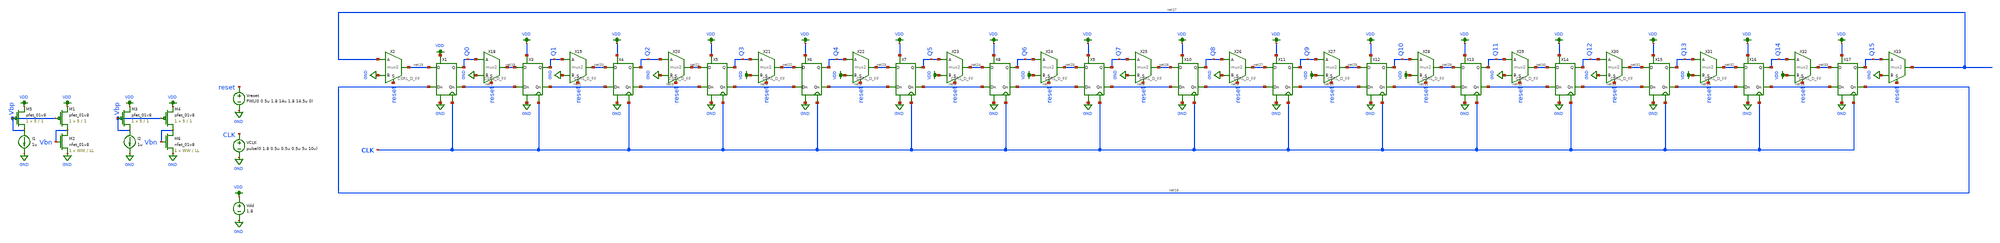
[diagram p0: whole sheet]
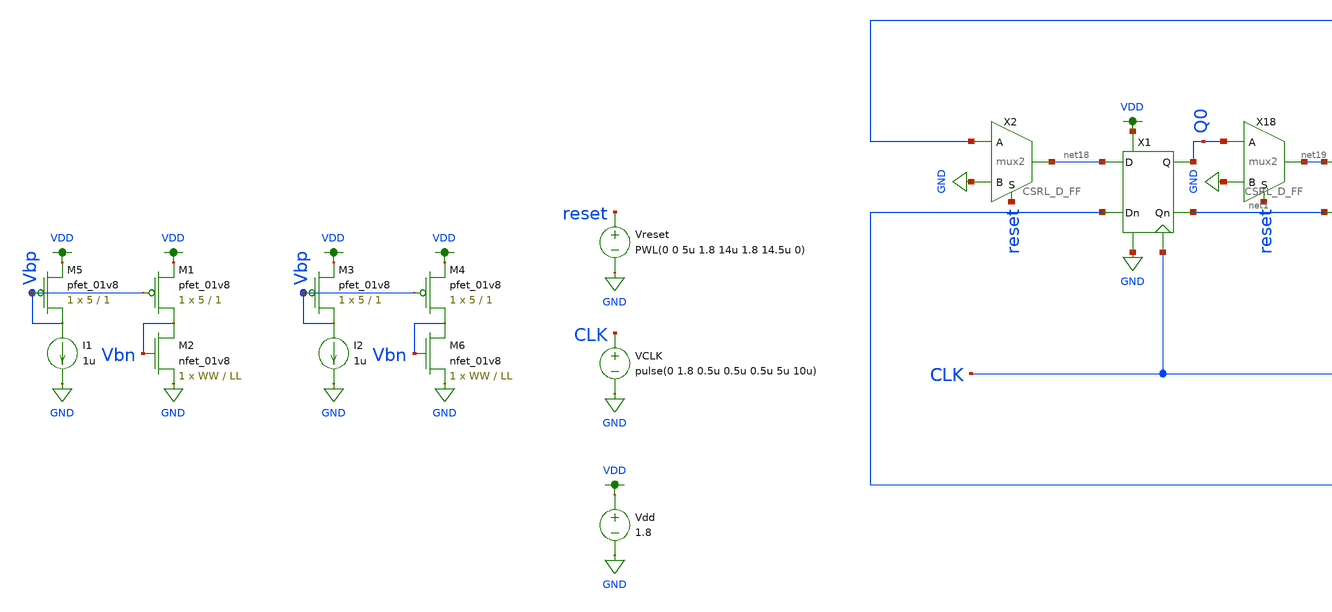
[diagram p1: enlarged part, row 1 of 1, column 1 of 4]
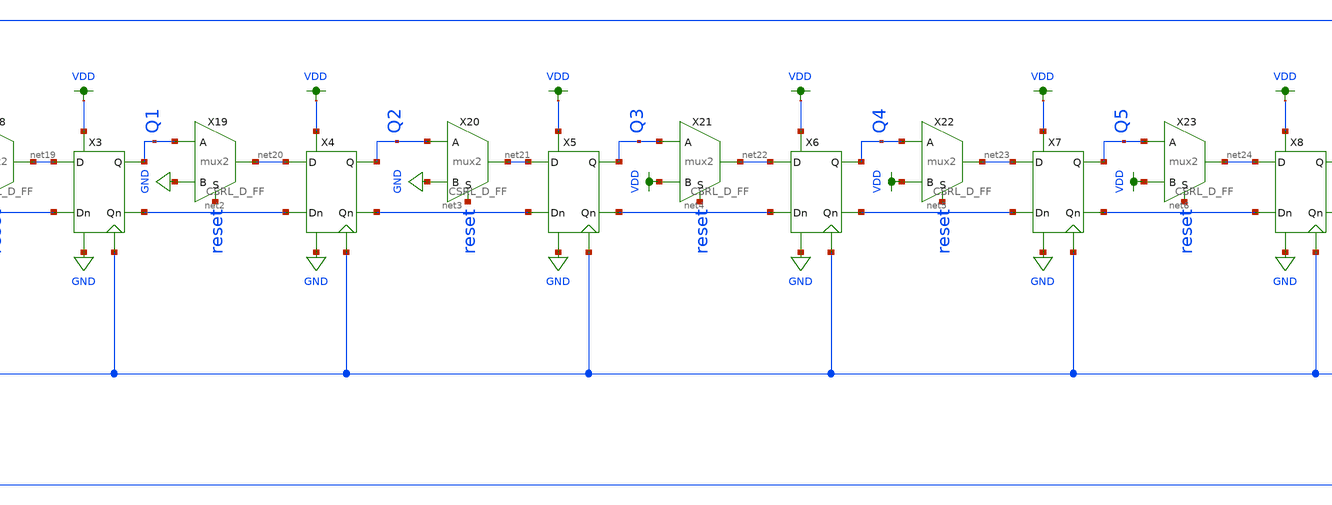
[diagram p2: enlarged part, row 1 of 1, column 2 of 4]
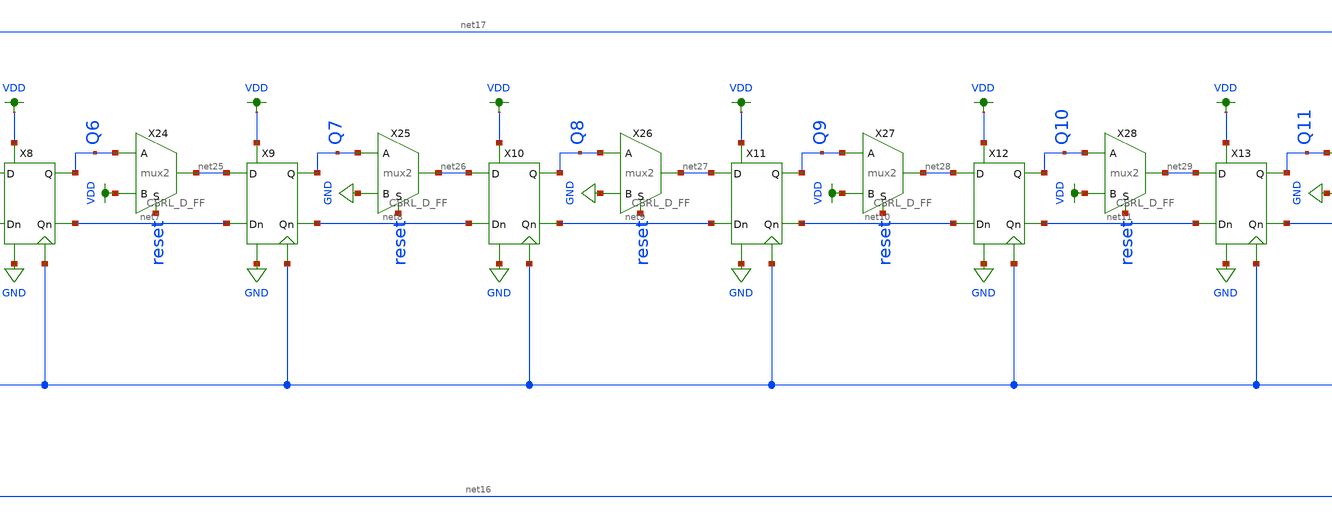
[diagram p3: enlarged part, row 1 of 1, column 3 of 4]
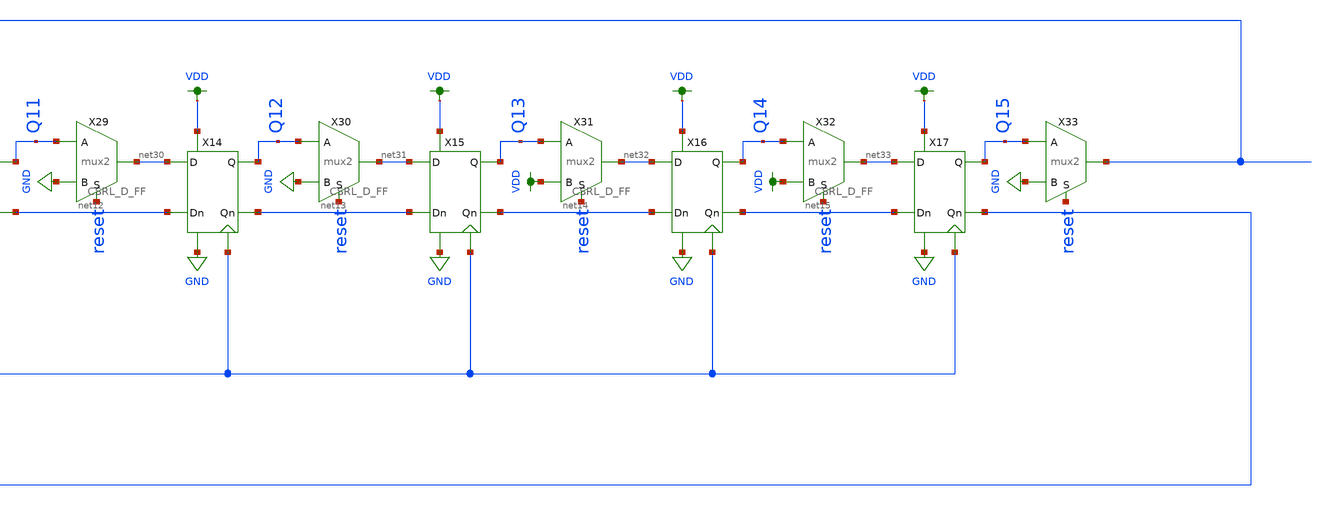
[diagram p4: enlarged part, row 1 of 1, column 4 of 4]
** sch_path: schematic/archive/phi1-new-circular-new.sch
**.subckt phi1-new-circular-new
VCLK CLK GND pulse(0 1.8 0.5u 0.5u 0.5u 5u 10u)
Vdd VDD GND 1.8
X3 net1 net19 net2 Q1 GND VDD CLK CSRL_D_FF
X4 net2 net20 net3 Q2 GND VDD CLK CSRL_D_FF
X5 net3 net21 net4 Q3 GND VDD CLK CSRL_D_FF
X6 net4 net22 net5 Q4 GND VDD CLK CSRL_D_FF
X7 net5 net23 net6 Q5 GND VDD CLK CSRL_D_FF
X8 net6 net24 net7 Q6 GND VDD CLK CSRL_D_FF
X9 net7 net25 net8 Q7 GND VDD CLK CSRL_D_FF
X10 net8 net26 net9 Q8 GND VDD CLK CSRL_D_FF
X11 net9 net27 net10 Q9 GND VDD CLK CSRL_D_FF
X12 net10 net28 net11 Q10 GND VDD CLK CSRL_D_FF
X13 net11 net29 net12 Q11 GND VDD CLK CSRL_D_FF
X14 net12 net30 net13 Q12 GND VDD CLK CSRL_D_FF
X15 net13 net31 net14 Q13 GND VDD CLK CSRL_D_FF
X16 net14 net32 net15 Q14 GND VDD CLK CSRL_D_FF
X17 net15 net33 net16 Q15 GND VDD CLK CSRL_D_FF
X1 net16 net18 net1 Q0 GND VDD CLK CSRL_D_FF
X2 net18 net17 GND reset mux2
X18 net19 Q0 GND reset mux2
X19 net20 Q1 GND reset mux2
X20 net21 Q2 GND reset mux2
X21 net22 Q3 VDD reset mux2
X22 net23 Q4 VDD reset mux2
X23 net24 Q5 VDD reset mux2
X24 net25 Q6 VDD reset mux2
X25 net26 Q7 GND reset mux2
X26 net27 Q8 GND reset mux2
X27 net28 Q9 VDD reset mux2
X28 net29 Q10 VDD reset mux2
X29 net30 Q11 GND reset mux2
X30 net31 Q12 GND reset mux2
X31 net32 Q13 VDD reset mux2
X32 net33 Q14 VDD reset mux2
X33 net17 Q15 GND reset mux2
XM5 Vbp Vbp VDD VDD sky130_fd_pr__pfet_01v8 L=1 W=5 nf=1 ad='int((nf+1)/2) * W/nf * 0.29' as='int((nf+2)/2) * W/nf * 0.29'
+ pd='2*int((nf+1)/2) * (W/nf + 0.29)' ps='2*int((nf+2)/2) * (W/nf + 0.29)' nrd='0.29 / W' nrs='0.29 / W'
+ sa=0 sb=0 sd=0 mult=1 m=1
I1 Vbp GND 1u
XM1 Vbn Vbp VDD VDD sky130_fd_pr__pfet_01v8 L=1 W=5 nf=1 ad='int((nf+1)/2) * W/nf * 0.29' as='int((nf+2)/2) * W/nf * 0.29'
+ pd='2*int((nf+1)/2) * (W/nf + 0.29)' ps='2*int((nf+2)/2) * (W/nf + 0.29)' nrd='0.29 / W' nrs='0.29 / W'
+ sa=0 sb=0 sd=0 mult=1 m=1
XM2 Vbn Vbn GND GND sky130_fd_pr__nfet_01v8 L=LL W=WW nf=1 ad='int((nf+1)/2) * W/nf * 0.29' as='int((nf+2)/2) * W/nf * 0.29'
+ pd='2*int((nf+1)/2) * (W/nf + 0.29)' ps='2*int((nf+2)/2) * (W/nf + 0.29)' nrd='0.29 / W' nrs='0.29 / W'
+ sa=0 sb=0 sd=0 mult=1 m=1
XM3 Vbp Vbp VDD VDD sky130_fd_pr__pfet_01v8 L=1 W=5 nf=1 ad='int((nf+1)/2) * W/nf * 0.29' as='int((nf+2)/2) * W/nf * 0.29'
+ pd='2*int((nf+1)/2) * (W/nf + 0.29)' ps='2*int((nf+2)/2) * (W/nf + 0.29)' nrd='0.29 / W' nrs='0.29 / W'
+ sa=0 sb=0 sd=0 mult=1 m=1
I2 Vbp GND 1u
XM4 Vbn Vbp VDD VDD sky130_fd_pr__pfet_01v8 L=1 W=5 nf=1 ad='int((nf+1)/2) * W/nf * 0.29' as='int((nf+2)/2) * W/nf * 0.29'
+ pd='2*int((nf+1)/2) * (W/nf + 0.29)' ps='2*int((nf+2)/2) * (W/nf + 0.29)' nrd='0.29 / W' nrs='0.29 / W'
+ sa=0 sb=0 sd=0 mult=1 m=1
XM6 Vbn Vbn GND GND sky130_fd_pr__nfet_01v8 L=LL W=WW nf=1 ad='int((nf+1)/2) * W/nf * 0.29' as='int((nf+2)/2) * W/nf * 0.29'
+ pd='2*int((nf+1)/2) * (W/nf + 0.29)' ps='2*int((nf+2)/2) * (W/nf + 0.29)' nrd='0.29 / W' nrs='0.29 / W'
+ sa=0 sb=0 sd=0 mult=1 m=1
Vreset reset GND PWL(0 0 5u 1.8 14u 1.8 14.5u 0)
**** begin user architecture code

.ic v(Q0)=0 v(Q1)=0 v(Q2)=0 v(Q3)=0 v(Q4)=1 v(Q5)=1 v(Q6)=1 v(Q7)=1 v(Q8)=0 v(Q9)=0 v(Q10)=1
+ v(Q11)=1 v(Q12)=0 v(Q13)=0 v(Q14)=1 v(Q15)=1
.tran 0.5u 50u
.save all


.option wnflag=1
.param MC_SWITCH=0.0
.lib ~/skywater/skywater-pdk/libraries/sky130_fd_pr_ngspice/latest/models/sky130.lib.spice tt

**** end user architecture code
**.ends

* expanding   symbol:  /home/madvlsi/Documents/MADVLSI-Final_Project/schematic/CSRL_D_FF.sym # of
*+ pins=7
** sym_path: schematic/CSRL_D_FF.sym
** sch_path: schematic/CSRL_D_FF.sch
.subckt CSRL_D_FF Dn D Qn Q VN VP CLK
*.ipin Dn
*.ipin D
*.iopin VP
*.iopin VN
*.iopin CLK
*.opin Qn
*.opin Q
XM1 net5 CLK VP VDD sky130_fd_pr__pfet_01v8 L=0.15 W=1 nf=1 ad='int((nf+1)/2) * W/nf * 0.29' as='int((nf+2)/2) * W/nf * 0.29'
+ pd='2*int((nf+1)/2) * (W/nf + 0.29)' ps='2*int((nf+2)/2) * (W/nf + 0.29)' nrd='0.29 / W' nrs='0.29 / W'
+ sa=0 sb=0 sd=0 mult=1 m=1
XM2 net6 CLK VP VDD sky130_fd_pr__pfet_01v8 L=0.15 W=1 nf=1 ad='int((nf+1)/2) * W/nf * 0.29' as='int((nf+2)/2) * W/nf * 0.29'
+ pd='2*int((nf+1)/2) * (W/nf + 0.29)' ps='2*int((nf+2)/2) * (W/nf + 0.29)' nrd='0.29 / W' nrs='0.29 / W'
+ sa=0 sb=0 sd=0 mult=1 m=1
XM3 net3 CLK Q GND sky130_fd_pr__nfet_01v8 L=0.15 W=1 nf=1 ad='int((nf+1)/2) * W/nf * 0.29' as='int((nf+2)/2) * W/nf * 0.29'
+ pd='2*int((nf+1)/2) * (W/nf + 0.29)' ps='2*int((nf+2)/2) * (W/nf + 0.29)' nrd='0.29 / W' nrs='0.29 / W'
+ sa=0 sb=0 sd=0 mult=1 m=1
XM4 net4 CLK Qn GND sky130_fd_pr__nfet_01v8 L=0.15 W=1 nf=1 ad='int((nf+1)/2) * W/nf * 0.29' as='int((nf+2)/2) * W/nf * 0.29'
+ pd='2*int((nf+1)/2) * (W/nf + 0.29)' ps='2*int((nf+2)/2) * (W/nf + 0.29)' nrd='0.29 / W' nrs='0.29 / W'
+ sa=0 sb=0 sd=0 mult=1 m=1
XM5 Q Qn net6 VDD sky130_fd_pr__pfet_01v8 L=0.15 W=1 nf=1 ad='int((nf+1)/2) * W/nf * 0.29' as='int((nf+2)/2) * W/nf * 0.29'
+ pd='2*int((nf+1)/2) * (W/nf + 0.29)' ps='2*int((nf+2)/2) * (W/nf + 0.29)' nrd='0.29 / W' nrs='0.29 / W'
+ sa=0 sb=0 sd=0 mult=1 m=1
XM6 VN Qn Q GND sky130_fd_pr__nfet_01v8 L=0.15 W=1 nf=1 ad='int((nf+1)/2) * W/nf * 0.29' as='int((nf+2)/2) * W/nf * 0.29'
+ pd='2*int((nf+1)/2) * (W/nf + 0.29)' ps='2*int((nf+2)/2) * (W/nf + 0.29)' nrd='0.29 / W' nrs='0.29 / W'
+ sa=0 sb=0 sd=0 mult=1 m=1
XM7 Qn Q net5 VDD sky130_fd_pr__pfet_01v8 L=0.15 W=1 nf=1 ad='int((nf+1)/2) * W/nf * 0.29' as='int((nf+2)/2) * W/nf * 0.29'
+ pd='2*int((nf+1)/2) * (W/nf + 0.29)' ps='2*int((nf+2)/2) * (W/nf + 0.29)' nrd='0.29 / W' nrs='0.29 / W'
+ sa=0 sb=0 sd=0 mult=1 m=1
XM8 VN Q Qn GND sky130_fd_pr__nfet_01v8 L=0.15 W=1 nf=1 ad='int((nf+1)/2) * W/nf * 0.29' as='int((nf+2)/2) * W/nf * 0.29'
+ pd='2*int((nf+1)/2) * (W/nf + 0.29)' ps='2*int((nf+2)/2) * (W/nf + 0.29)' nrd='0.29 / W' nrs='0.29 / W'
+ sa=0 sb=0 sd=0 mult=1 m=1
XM9 net4 CLK Dn VDD sky130_fd_pr__pfet_01v8 L=0.15 W=1 nf=1 ad='int((nf+1)/2) * W/nf * 0.29' as='int((nf+2)/2) * W/nf * 0.29'
+ pd='2*int((nf+1)/2) * (W/nf + 0.29)' ps='2*int((nf+2)/2) * (W/nf + 0.29)' nrd='0.29 / W' nrs='0.29 / W'
+ sa=0 sb=0 sd=0 mult=1 m=1
XM10 net3 CLK D VDD sky130_fd_pr__pfet_01v8 L=0.15 W=1 nf=1 ad='int((nf+1)/2) * W/nf * 0.29' as='int((nf+2)/2) * W/nf * 0.29'
+ pd='2*int((nf+1)/2) * (W/nf + 0.29)' ps='2*int((nf+2)/2) * (W/nf + 0.29)' nrd='0.29 / W' nrs='0.29 / W'
+ sa=0 sb=0 sd=0 mult=1 m=1
XM11 VN CLK net1 GND sky130_fd_pr__nfet_01v8 L=0.15 W=1 nf=1 ad='int((nf+1)/2) * W/nf * 0.29' as='int((nf+2)/2) * W/nf * 0.29'
+ pd='2*int((nf+1)/2) * (W/nf + 0.29)' ps='2*int((nf+2)/2) * (W/nf + 0.29)' nrd='0.29 / W' nrs='0.29 / W'
+ sa=0 sb=0 sd=0 mult=1 m=1
XM12 VN CLK net2 GND sky130_fd_pr__nfet_01v8 L=0.15 W=1 nf=1 ad='int((nf+1)/2) * W/nf * 0.29' as='int((nf+2)/2) * W/nf * 0.29'
+ pd='2*int((nf+1)/2) * (W/nf + 0.29)' ps='2*int((nf+2)/2) * (W/nf + 0.29)' nrd='0.29 / W' nrs='0.29 / W'
+ sa=0 sb=0 sd=0 mult=1 m=1
XM13 VP net3 net4 VDD sky130_fd_pr__pfet_01v8 L=0.15 W=1 nf=1 ad='int((nf+1)/2) * W/nf * 0.29' as='int((nf+2)/2) * W/nf * 0.29'
+ pd='2*int((nf+1)/2) * (W/nf + 0.29)' ps='2*int((nf+2)/2) * (W/nf + 0.29)' nrd='0.29 / W' nrs='0.29 / W'
+ sa=0 sb=0 sd=0 mult=1 m=1
XM14 VP net4 net3 VDD sky130_fd_pr__pfet_01v8 L=0.15 W=1 nf=1 ad='int((nf+1)/2) * W/nf * 0.29' as='int((nf+2)/2) * W/nf * 0.29'
+ pd='2*int((nf+1)/2) * (W/nf + 0.29)' ps='2*int((nf+2)/2) * (W/nf + 0.29)' nrd='0.29 / W' nrs='0.29 / W'
+ sa=0 sb=0 sd=0 mult=1 m=1
XM15 net3 net4 net1 GND sky130_fd_pr__nfet_01v8 L=0.15 W=1 nf=1 ad='int((nf+1)/2) * W/nf * 0.29' as='int((nf+2)/2) * W/nf * 0.29'
+ pd='2*int((nf+1)/2) * (W/nf + 0.29)' ps='2*int((nf+2)/2) * (W/nf + 0.29)' nrd='0.29 / W' nrs='0.29 / W'
+ sa=0 sb=0 sd=0 mult=1 m=1
XM16 net4 net3 net2 GND sky130_fd_pr__nfet_01v8 L=0.15 W=1 nf=1 ad='int((nf+1)/2) * W/nf * 0.29' as='int((nf+2)/2) * W/nf * 0.29'
+ pd='2*int((nf+1)/2) * (W/nf + 0.29)' ps='2*int((nf+2)/2) * (W/nf + 0.29)' nrd='0.29 / W' nrs='0.29 / W'
+ sa=0 sb=0 sd=0 mult=1 m=1
XM17 VN CLK net2 GND sky130_fd_pr__nfet_01v8 L=0.15 W=1 nf=1 ad='int((nf+1)/2) * W/nf * 0.29' as='int((nf+2)/2) * W/nf * 0.29'
+ pd='2*int((nf+1)/2) * (W/nf + 0.29)' ps='2*int((nf+2)/2) * (W/nf + 0.29)' nrd='0.29 / W' nrs='0.29 / W'
+ sa=0 sb=0 sd=0 mult=1 m=1
XM18 VN CLK net1 GND sky130_fd_pr__nfet_01v8 L=0.15 W=1 nf=1 ad='int((nf+1)/2) * W/nf * 0.29' as='int((nf+2)/2) * W/nf * 0.29'
+ pd='2*int((nf+1)/2) * (W/nf + 0.29)' ps='2*int((nf+2)/2) * (W/nf + 0.29)' nrd='0.29 / W' nrs='0.29 / W'
+ sa=0 sb=0 sd=0 mult=1 m=1
.ends


* expanding   symbol:  /home/madvlsi/Documents/MADVLSI-Final_Project/schematic/mux2.sym # of pins=4
** sym_path: /home/madvlsi/Documents/MADVLSI-Final_Project/schematic/mux2.sym
** sch_path: /home/madvlsi/Documents/MADVLSI-Final_Project/schematic/mux2.sch
.subckt mux2 Y A B S
*.opin Y
*.ipin B
*.ipin A
*.ipin S
XM1 Y net1 A VDD sky130_fd_pr__pfet_01v8 L=0.15 W=1 nf=1 ad='int((nf+1)/2) * W/nf * 0.29' as='int((nf+2)/2) * W/nf * 0.29'
+ pd='2*int((nf+1)/2) * (W/nf + 0.29)' ps='2*int((nf+2)/2) * (W/nf + 0.29)' nrd='0.29 / W' nrs='0.29 / W'
+ sa=0 sb=0 sd=0 mult=1 m=1
XM2 Y S B VDD sky130_fd_pr__pfet_01v8 L=0.15 W=1 nf=1 ad='int((nf+1)/2) * W/nf * 0.29' as='int((nf+2)/2) * W/nf * 0.29'
+ pd='2*int((nf+1)/2) * (W/nf + 0.29)' ps='2*int((nf+2)/2) * (W/nf + 0.29)' nrd='0.29 / W' nrs='0.29 / W'
+ sa=0 sb=0 sd=0 mult=1 m=1
XM3 Y net1 B GND sky130_fd_pr__nfet_01v8 L=0.15 W=1 nf=1 ad='int((nf+1)/2) * W/nf * 0.29' as='int((nf+2)/2) * W/nf * 0.29'
+ pd='2*int((nf+1)/2) * (W/nf + 0.29)' ps='2*int((nf+2)/2) * (W/nf + 0.29)' nrd='0.29 / W' nrs='0.29 / W'
+ sa=0 sb=0 sd=0 mult=1 m=1
XM4 Y S A GND sky130_fd_pr__nfet_01v8 L=0.15 W=1 nf=1 ad='int((nf+1)/2) * W/nf * 0.29' as='int((nf+2)/2) * W/nf * 0.29'
+ pd='2*int((nf+1)/2) * (W/nf + 0.29)' ps='2*int((nf+2)/2) * (W/nf + 0.29)' nrd='0.29 / W' nrs='0.29 / W'
+ sa=0 sb=0 sd=0 mult=1 m=1
X1 S net1 VDD GND inverter
.ends


* expanding   symbol:  /home/madvlsi/Documents/MADVLSI-Final_Project/schematic/inverter.sym # of
*+ pins=4
** sym_path: schematic/inverter.sym
** sch_path: schematic/inverter.sch
.subckt inverter A Y VP VN
*.opin Y
*.ipin A
*.iopin VP
*.iopin VN
XM3 Y A VP VDD sky130_fd_pr__pfet_01v8 L={Lp} W={Wp} nf=1 ad='int((nf+1)/2) * W/nf * 0.29' as='int((nf+2)/2) * W/nf * 0.29'
+ pd='2*int((nf+1)/2) * (W/nf + 0.29)' ps='2*int((nf+2)/2) * (W/nf + 0.29)' nrd='0.29 / W' nrs='0.29 / W'
+ sa=0 sb=0 sd=0 mult=1 m=1
XM4 Y A VP VDD sky130_fd_pr__pfet_01v8 L={Lp} W={Wp} nf=1 ad='int((nf+1)/2) * W/nf * 0.29' as='int((nf+2)/2) * W/nf * 0.29'
+ pd='2*int((nf+1)/2) * (W/nf + 0.29)' ps='2*int((nf+2)/2) * (W/nf + 0.29)' nrd='0.29 / W' nrs='0.29 / W'
+ sa=0 sb=0 sd=0 mult=1 m=1
XM5 Y A VN GND sky130_fd_pr__nfet_01v8 L={Lp} W={Wp} nf=1 ad='int((nf+1)/2) * W/nf * 0.29' as='int((nf+2)/2) * W/nf * 0.29'
+ pd='2*int((nf+1)/2) * (W/nf + 0.29)' ps='2*int((nf+2)/2) * (W/nf + 0.29)' nrd='0.29 / W' nrs='0.29 / W'
+ sa=0 sb=0 sd=0 mult=1 m=1
.ends

.GLOBAL GND
.GLOBAL VDD
.end
